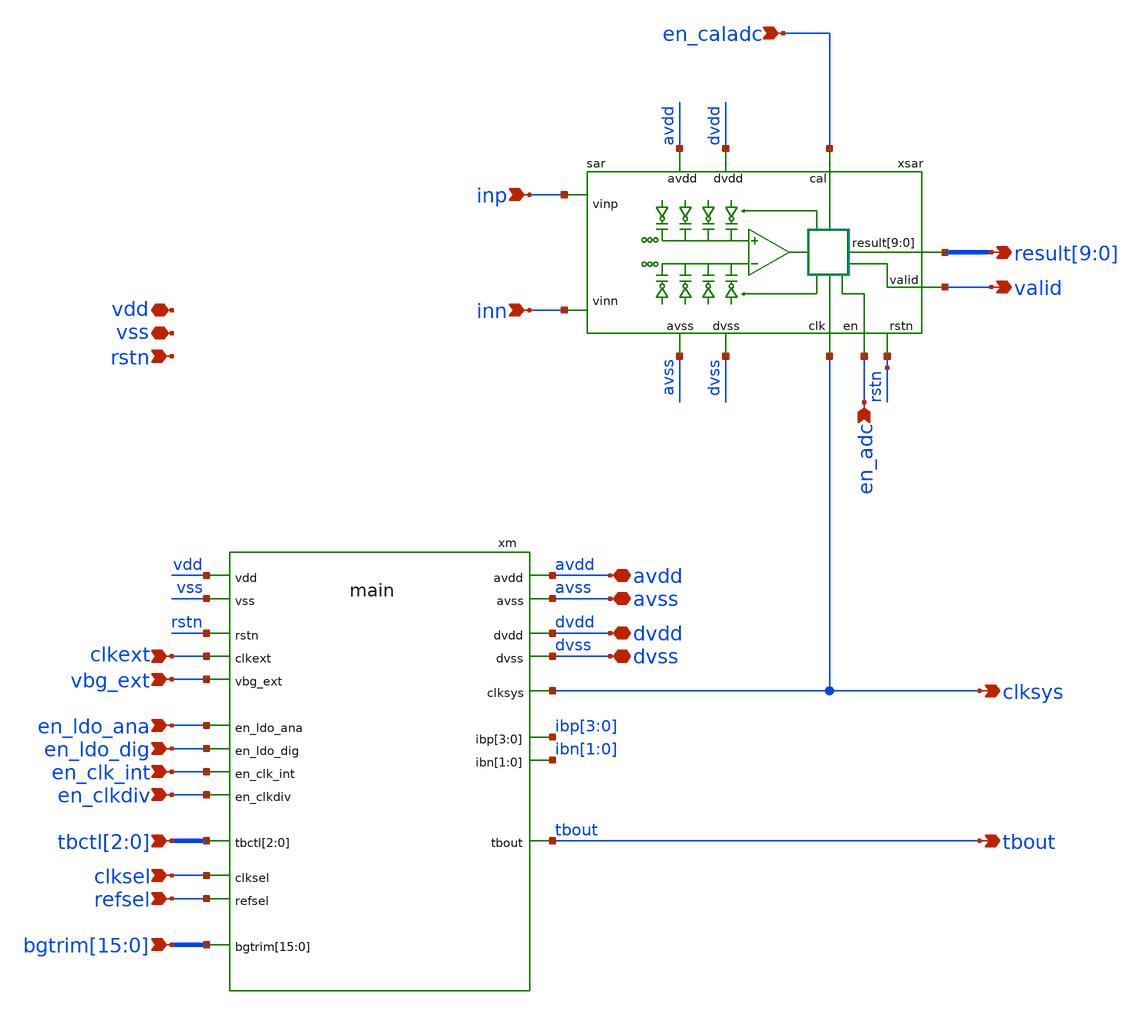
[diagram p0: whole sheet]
** sch_path: xschem/top/top.sch
**.subckt top inp inn clksel clkext en_caladc en_adc en_clkdiv clksys en_ldo_ana en_ldo_dig
*+ result[9],result[8],result[7],result[6],result[5],result[4],result[3],result[2],result[1],result[0] valid refsel vdd vss rstn vbg_ext en_clk_int avdd dvdd tbout avss dvss
*+ bgtrim[15],bgtrim[14],bgtrim[13],bgtrim[12],bgtrim[11],bgtrim[10],bgtrim[9],bgtrim[8],bgtrim[7],bgtrim[6],bgtrim[5],bgtrim[4],bgtrim[3],bgtrim[2],bgtrim[1],bgtrim[0] tbctl[2],tbctl[1],tbctl[0]
*.ipin inp
*.ipin inn
*.ipin clksel
*.ipin clkext
*.ipin en_caladc
*.ipin en_adc
*.ipin en_clkdiv
*.opin clksys
*.ipin en_ldo_ana
*.ipin en_ldo_dig
*.opin
*+ result[9],result[8],result[7],result[6],result[5],result[4],result[3],result[2],result[1],result[0]
*.opin valid
*.ipin refsel
*.iopin vdd
*.iopin vss
*.ipin rstn
*.ipin vbg_ext
*.ipin en_clk_int
*.iopin avdd
*.iopin dvdd
*.opin tbout
*.iopin avss
*.iopin dvss
*.ipin
*+ bgtrim[15],bgtrim[14],bgtrim[13],bgtrim[12],bgtrim[11],bgtrim[10],bgtrim[9],bgtrim[8],bgtrim[7],bgtrim[6],bgtrim[5],bgtrim[4],bgtrim[3],bgtrim[2],bgtrim[1],bgtrim[0]
*.ipin tbctl[2],tbctl[1],tbctl[0]
xm dvdd en_ldo_dig avdd rstn vdd vss en_ldo_ana clksys en_clk_int clkext ibp[3] ibp[2] ibp[1] ibp[0]
+ ibn[1] ibn[0] en_clkdiv clksel refsel vbg_ext avss dvss tbout bgtrim[15] bgtrim[14] bgtrim[13] bgtrim[12]
+ bgtrim[11] bgtrim[10] bgtrim[9] bgtrim[8] bgtrim[7] bgtrim[6] bgtrim[5] bgtrim[4] bgtrim[3] bgtrim[2]
+ bgtrim[1] bgtrim[0] tbctl[2] tbctl[1] tbctl[0] main
xsar avdd dvdd dvss result[9] result[8] result[7] result[6] result[5] result[4] result[3] result[2]
+ result[1] result[0] inn avss clksys inp en_adc valid en_caladc rstn sar
**.ends
.end
